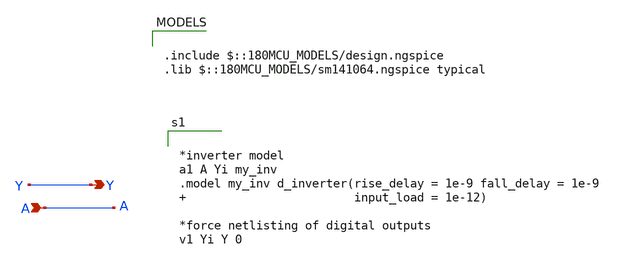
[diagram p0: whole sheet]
** sch_path: XSCHEM Files/inv.sch
**.subckt inv A Y
*.ipin A
*.opin Y
**** begin user architecture code


*inverter model
a1 A Yi my_inv
.model my_inv d_inverter(rise_delay = 1e-9 fall_delay = 1e-9                         input_load =
+ 1e-12)

*force netlisting of digital outputs
v1 Yi Y 0



.include $::180MCU_MODELS/design.ngspice
.lib $::180MCU_MODELS/sm141064.ngspice typical

**** end user architecture code
**.ends
.end
